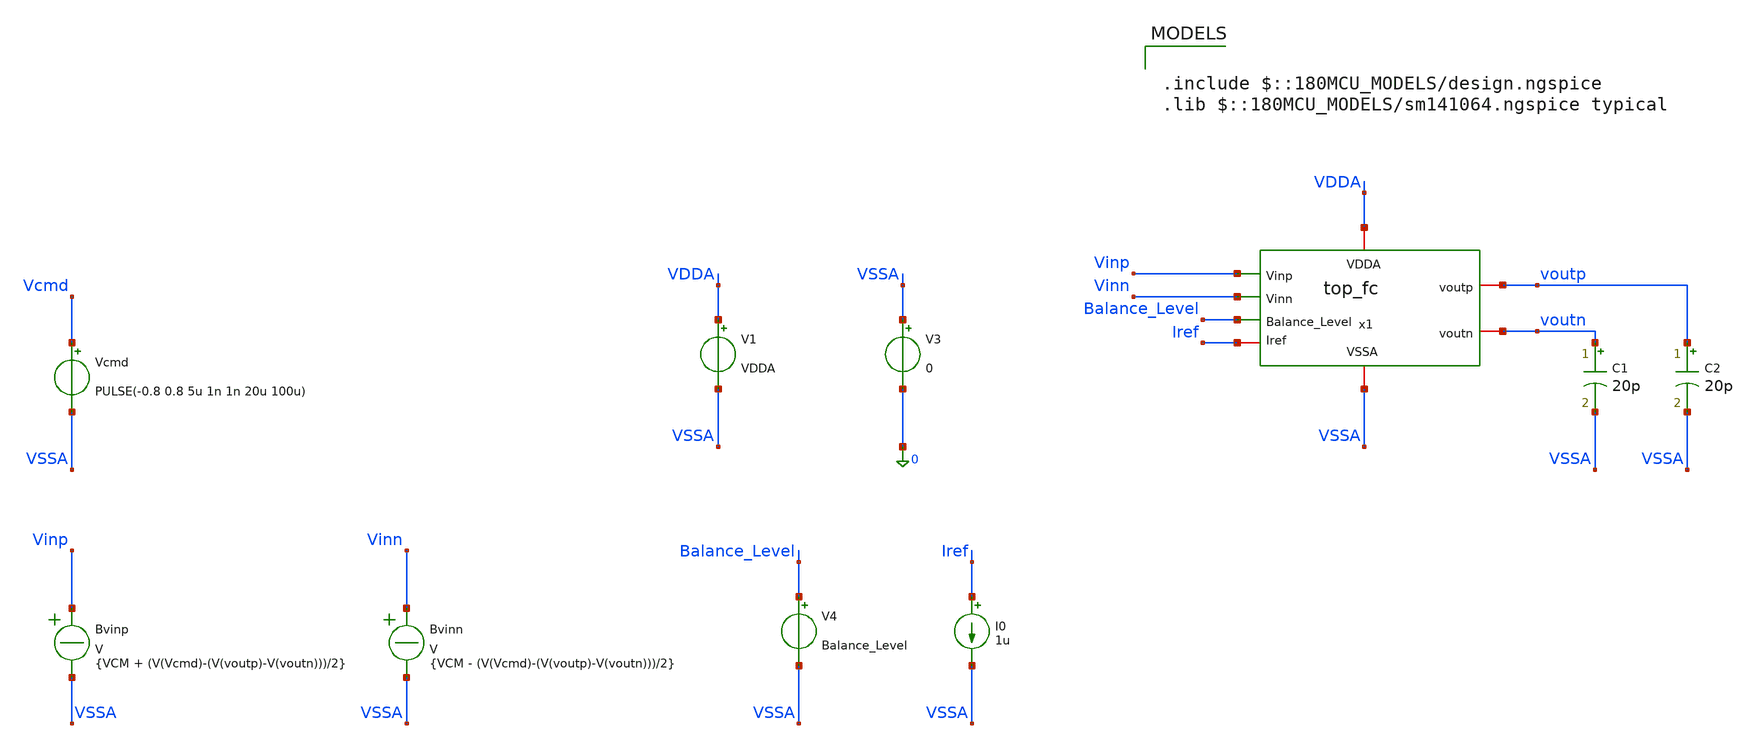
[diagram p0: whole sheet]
** sch_path: Folded_cascode/testbenches/top_fc_setting_tb.sch
**.subckt top_fc_setting_tb
x1 Balance_Level Vinp voutp VDDA voutn Vinn Iref VSSA top_fc
C1 voutn VSSA 20p m=1
C2 voutp VSSA 20p m=1
V1 VDDA VSSA VDDA
V3 VSSA 0 0
V4 Balance_Level VSSA Balance_Level
I0 Iref VSSA 1u
Bvinp Vinp VSSA V = {VCM + (V(Vcmd)-(V(voutp)-V(voutn)))/2}
Bvinn Vinn VSSA V = {VCM - (V(Vcmd)-(V(voutp)-V(voutn)))/2}
Vcmd Vcmd VSSA PULSE(-0.8 0.8 5u 1n 1n 20u 100u)
**** begin user architecture code

.include $::180MCU_MODELS/design.ngspice
.lib $::180MCU_MODELS/sm141064.ngspice typical



.temp 27
.param VDDA = 5
.param Balance_Level = 1.5
.param VD = 0
.param VCM = 2.5

.control
option sparse
set filetype=ascii
set wr_singlescale
set wr_vecnames
save all
save @m.x1.x1.xm1.m0[id]
save @m.x1.x1.xm1.m0[gm]
save @m.x1.x1.xm1.m0[vgs]
save @m.x1.x1.xm1.m0[vds]
save @m.x1.x1.xm1.m0[vth]
save @m.x1.x1.xm1.m0[gds]
save @m.x1.x1.xm1.m0[vdsat]

save @m.x1.x1.xm2.m0[id]
save @m.x1.x1.xm2.m0[gm]
save @m.x1.x1.xm2.m0[vgs]
save @m.x1.x1.xm2.m0[vds]
save @m.x1.x1.xm2.m0[vth]
save @m.x1.x1.xm2.m0[gds]
save @m.x1.x1.xm2.m0[vdsat]

save @m.x1.x1.xm9.m0[id]
save @m.x1.x1.xm9.m0[gm]
save @m.x1.x1.xm9.m0[vgs]
save @m.x1.x1.xm9.m0[vds]
save @m.x1.x1.xm9.m0[vth]
save @m.x1.x1.xm9.m0[gds]
save @m.x1.x1.xm9.m0[vdsat]

save @m.x1.x1.xm8.m0[id]
save @m.x1.x1.xm8.m0[gm]
save @m.x1.x1.xm8.m0[vgs]
save @m.x1.x1.xm8.m0[vds]
save @m.x1.x1.xm8.m0[vth]
save @m.x1.x1.xm8.m0[gds]
save @m.x1.x1.xm8.m0[vdsat]

save @m.x1.x1.xm6.m0[id]
save @m.x1.x1.xm6.m0[gm]
save @m.x1.x1.xm6.m0[vgs]
save @m.x1.x1.xm6.m0[vds]
save @m.x1.x1.xm6.m0[vth]
save @m.x1.x1.xm6.m0[gds]
save @m.x1.x1.xm6.m0[vdsat]

save @m.x1.x1.xm5.m0[id]
save @m.x1.x1.xm5.m0[gm]
save @m.x1.x1.xm5.m0[vgs]
save @m.x1.x1.xm5.m0[vds]
save @m.x1.x1.xm5.m0[vth]
save @m.x1.x1.xm5.m0[gds]
save @m.x1.x1.xm5.m0[vdsat]

save @m.x1.x2.xm1.m0[id]
save @m.x1.x2.xm1.m0[gm]
save @m.x1.x2.xm1.m0[vgs]
save @m.x1.x2.xm1.m0[vds]
save @m.x1.x2.xm1.m0[vth]
save @m.x1.x2.xm1.m0[gds]

save @m.x1.x2.xm2.m0[id]
save @m.x1.x2.xm2.m0[gm]
save @m.x1.x2.xm2.m0[vgs]
save @m.x1.x2.xm2.m0[vds]
save @m.x1.x2.xm2.m0[vth]
save @m.x1.x2.xm2.m0[gds]

save @m.x1.x2.xm3.m0[id]
save @m.x1.x2.xm3.m0[gm]
save @m.x1.x2.xm3.m0[vgs]
save @m.x1.x2.xm3.m0[vds]
save @m.x1.x2.xm3.m0[vth]
save @m.x1.x2.xm3.m0[gds]

save @m.x1.x2.xm4.m0[id]
save @m.x1.x2.xm4.m0[gm]
save @m.x1.x2.xm4.m0[vgs]
save @m.x1.x2.xm4.m0[vds]
save @m.x1.x2.xm4.m0[vth]
save @m.x1.x2.xm4.m0[gds]

save @m.x1.x2.xm5.m0[id]
save @m.x1.x2.xm5.m0[gm]
save @m.x1.x2.xm5.m0[vgs]
save @m.x1.x2.xm5.m0[vds]
save @m.x1.x2.xm5.m0[vth]
save @m.x1.x2.xm5.m0[gds]

save @m.x1.x2.xm6.m0[id]
save @m.x1.x2.xm6.m0[gm]
save @m.x1.x2.xm6.m0[vgs]
save @m.x1.x2.xm6.m0[vds]
save @m.x1.x2.xm6.m0[vth]
save @m.x1.x2.xm6.m0[gds]

save @m.x1.x2.xm7.m0[id]
save @m.x1.x2.xm7.m0[gm]
save @m.x1.x2.xm7.m0[vgs]
save @m.x1.x2.xm7.m0[vds]
save @m.x1.x2.xm7.m0[vth]
save @m.x1.x2.xm7.m0[gds]

save @m.x1.x2.xm8.m0[id]
save @m.x1.x2.xm8.m0[gm]
save @m.x1.x2.xm8.m0[vgs]
save @m.x1.x2.xm8.m0[vds]
save @m.x1.x2.xm8.m0[vth]
save @m.x1.x2.xm8.m0[gds]

save @m.x1.x2.xm9.m0[id]
save @m.x1.x2.xm9.m0[gm]
save @m.x1.x2.xm9.m0[vgs]
save @m.x1.x2.xm9.m0[vds]
save @m.x1.x2.xm9.m0[vth]
save @m.x1.x2.xm9.m0[gds]

save @m.x1.x3.xm1.m0[id]
save @m.x1.x3.xm1.m0[gm]
save @m.x1.x3.xm1.m0[vgs]
save @m.x1.x3.xm1.m0[vds]
save @m.x1.x3.xm1.m0[vth]
save @m.x1.x3.xm1.m0[gds]

save @m.x1.x3.xm2.m0[id]
save @m.x1.x3.xm2.m0[gm]
save @m.x1.x3.xm2.m0[vgs]
save @m.x1.x3.xm2.m0[vds]
save @m.x1.x3.xm2.m0[vth]
save @m.x1.x3.xm2.m0[gds]

save @m.x1.x3.xm3.m0[id]
save @m.x1.x3.xm3.m0[gm]
save @m.x1.x3.xm3.m0[vgs]
save @m.x1.x3.xm3.m0[vds]
save @m.x1.x3.xm3.m0[vth]
save @m.x1.x3.xm3.m0[gds]

save @m.x1.x3.xm4.m0[id]
save @m.x1.x3.xm4.m0[gm]
save @m.x1.x3.xm4.m0[vgs]
save @m.x1.x3.xm4.m0[vds]
save @m.x1.x3.xm4.m0[vth]
save @m.x1.x3.xm4.m0[gds]

save @m.x1.x3.xm5.m0[id]
save @m.x1.x3.xm5.m0[gm]
save @m.x1.x3.xm5.m0[vgs]
save @m.x1.x3.xm5.m0[vds]
save @m.x1.x3.xm5.m0[vth]
save @m.x1.x3.xm5.m0[gds]

save @m.x1.x3.xm6.m0[id]
save @m.x1.x3.xm6.m0[gm]
save @m.x1.x3.xm6.m0[vgs]
save @m.x1.x3.xm6.m0[vds]
save @m.x1.x3.xm6.m0[vth]
save @m.x1.x3.xm6.m0[gds]

save @m.x1.x3.xm7.m0[id]
save @m.x1.x3.xm7.m0[gm]
save @m.x1.x3.xm7.m0[vgs]
save @m.x1.x3.xm7.m0[vds]
save @m.x1.x3.xm7.m0[vth]
save @m.x1.x3.xm7.m0[gds]

save @m.x1.x3.xm8.m0[id]
save @m.x1.x3.xm8.m0[gm]
save @m.x1.x3.xm8.m0[vgs]
save @m.x1.x3.xm8.m0[vds]
save @m.x1.x3.xm8.m0[vth]
save @m.x1.x3.xm8.m0[gds]

save @m.x1.x3.xm9.m0[id]
save @m.x1.x3.xm9.m0[gm]
save @m.x1.x3.xm9.m0[vgs]
save @m.x1.x3.xm9.m0[vds]
save @m.x1.x3.xm9.m0[vth]
save @m.x1.x3.xm9.m0[gds]

save @m.x1.x3.xm10.m0[id]
save @m.x1.x3.xm10.m0[gm]
save @m.x1.x3.xm10.m0[vgs]
save @m.x1.x3.xm10.m0[vds]
save @m.x1.x3.xm10.m0[vth]
save @m.x1.x3.xm10.m0[gds]

save @m.x1.x3.xm11.m0[id]
save @m.x1.x3.xm11.m0[gm]
save @m.x1.x3.xm11.m0[vgs]
save @m.x1.x3.xm11.m0[vds]
save @m.x1.x3.xm11.m0[vth]
save @m.x1.x3.xm11.m0[gds]

save @m.x1.x3.xm12.m0[id]
save @m.x1.x3.xm12.m0[gm]
save @m.x1.x3.xm12.m0[vgs]
save @m.x1.x3.xm12.m0[vds]
save @m.x1.x3.xm12.m0[vth]
save @m.x1.x3.xm12.m0[gds]

save @m.x1.x3.xm13.m0[id]
save @m.x1.x3.xm13.m0[gm]
save @m.x1.x3.xm13.m0[vgs]
save @m.x1.x3.xm13.m0[vds]
save @m.x1.x3.xm13.m0[vth]
save @m.x1.x3.xm13.m0[gds]

save @m.x1.x3.xm14.m0[id]
save @m.x1.x3.xm14.m0[gm]
save @m.x1.x3.xm14.m0[vgs]
save @m.x1.x3.xm14.m0[vds]
save @m.x1.x3.xm14.m0[vth]
save @m.x1.x3.xm14.m0[gds]

save @m.x1.x3.xm15.m0[id]
save @m.x1.x3.xm15.m0[gm]
save @m.x1.x3.xm15.m0[vgs]
save @m.x1.x3.xm15.m0[vds]
save @m.x1.x3.xm15.m0[vth]
save @m.x1.x3.xm15.m0[gds]

save @m.x1.x3.xm16.m0[id]
save @m.x1.x3.xm16.m0[gm]
save @m.x1.x3.xm16.m0[vgs]
save @m.x1.x3.xm16.m0[vds]
save @m.x1.x3.xm16.m0[vth]
save @m.x1.x3.xm16.m0[gds]

save @m.x1.x3.xm17.m0[id]
save @m.x1.x3.xm17.m0[gm]
save @m.x1.x3.xm17.m0[vgs]
save @m.x1.x3.xm17.m0[vds]
save @m.x1.x3.xm17.m0[vth]
save @m.x1.x3.xm17.m0[gds]

save @m.x1.x3.xm18.m0[id]
save @m.x1.x3.xm18.m0[gm]
save @m.x1.x3.xm18.m0[vgs]
save @m.x1.x3.xm18.m0[vds]
save @m.x1.x3.xm18.m0[vth]
save @m.x1.x3.xm18.m0[gds]

save @m.x1.x3.xm21.m0[id]
save @m.x1.x3.xm21.m0[gm]
save @m.x1.x3.xm21.m0[vgs]
save @m.x1.x3.xm21.m0[vds]
save @m.x1.x3.xm21.m0[vth]
save @m.x1.x3.xm21.m0[gds]

save @m.x1.x3.xm22.m0[id]
save @m.x1.x3.xm22.m0[gm]
save @m.x1.x3.xm22.m0[vgs]
save @m.x1.x3.xm22.m0[vds]
save @m.x1.x3.xm22.m0[vth]
save @m.x1.x3.xm22.m0[gds]

op
write top_fc_op_tb.raw all


* ------------------------------------------------------------
* Transient simulation
*
* 1 ns max timestep gives better resolution than the
* 10 ns step used for the slew-rate extraction.
* ------------------------------------------------------------

tran 1n 45u


* ------------------------------------------------------------
* Quantities
* ------------------------------------------------------------

let vod = v(voutp)-v(voutn)
let vocm = (v(voutp)+v(voutn))/2

let tracking_error = vod-v(Vcmd)


* ------------------------------------------------------------
* Save raw transient
* ------------------------------------------------------------

write top_fc_settling_tb.raw


* ------------------------------------------------------------
* Export for Python post-processing
*
* Columns:
*
* time
* Vcmd
* Vod
* Voutp
* Voutn
* Vocm
* tracking_error
* ------------------------------------------------------------

wrdata settling.dat v(Vcmd) vod v(voutp) v(voutn) vocm tracking_error


* ------------------------------------------------------------
* Diagnostic plots
* ------------------------------------------------------------

plot v(Vcmd) vod
plot tracking_error
plot v(voutp) v(voutn)
plot vocm

.endc


**** end user architecture code
**.ends
.end
